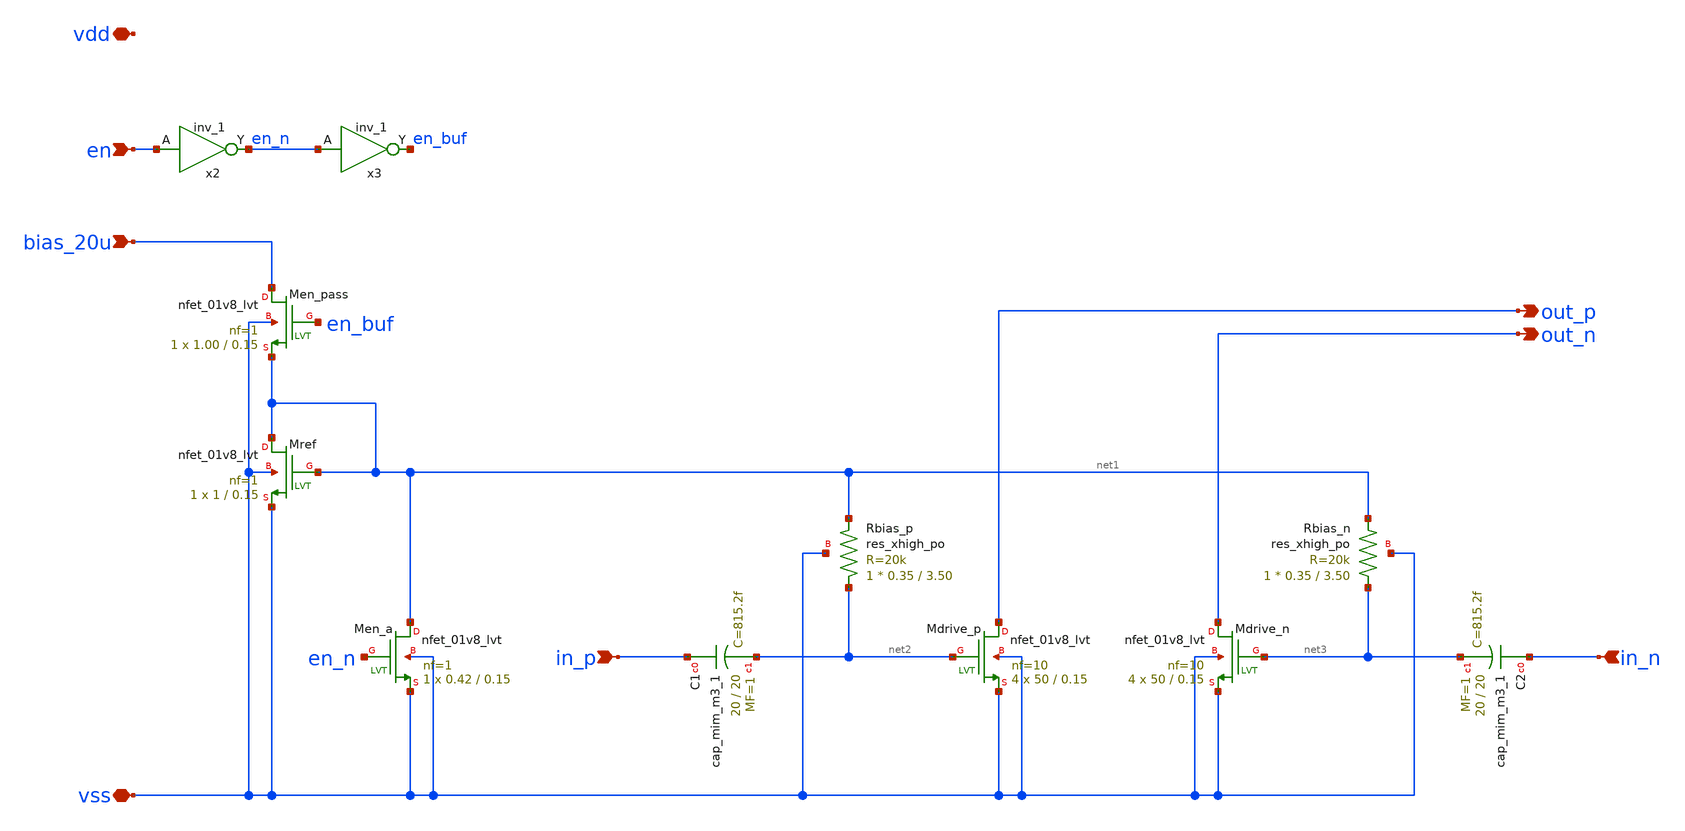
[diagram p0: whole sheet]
** sch_path: design/io_driver/io_driver.sch
**.subckt io_driver en bias_20u vss vdd out_p out_n in_n in_p
*.ipin en
*.ipin bias_20u
*.iopin vss
*.iopin vdd
*.opin out_p
*.opin out_n
*.ipin in_n
*.ipin in_p
XMdrive_p out_p net2 vss vss sky130_fd_pr__nfet_01v8_lvt L=0.15 W=50 nf=10 ad='int((nf+1)/2) * W/nf * 0.29'
+ as='int((nf+2)/2) * W/nf * 0.29' pd='2*int((nf+1)/2) * (W/nf + 0.29)' ps='2*int((nf+2)/2) * (W/nf + 0.29)'
+ nrd='0.29 / W' nrs='0.29 / W' sa=0 sb=0 sd=0 mult=4 m=4
XMdrive_n out_n net3 vss vss sky130_fd_pr__nfet_01v8_lvt L=0.15 W=50 nf=10 ad='int((nf+1)/2) * W/nf * 0.29'
+ as='int((nf+2)/2) * W/nf * 0.29' pd='2*int((nf+1)/2) * (W/nf + 0.29)' ps='2*int((nf+2)/2) * (W/nf + 0.29)'
+ nrd='0.29 / W' nrs='0.29 / W' sa=0 sb=0 sd=0 mult=4 m=4
XMref net1 net1 vss vss sky130_fd_pr__nfet_01v8_lvt L=0.15 W=1 nf=1 ad='int((nf+1)/2) * W/nf * 0.29'
+ as='int((nf+2)/2) * W/nf * 0.29' pd='2*int((nf+1)/2) * (W/nf + 0.29)' ps='2*int((nf+2)/2) * (W/nf + 0.29)'
+ nrd='0.29 / W' nrs='0.29 / W' sa=0 sb=0 sd=0 mult=1 m=1
XMen_pass bias_20u en_buf net1 vss sky130_fd_pr__nfet_01v8_lvt L=0.15 W=1.00 nf=1 ad='int((nf+1)/2) * W/nf * 0.29'
+ as='int((nf+2)/2) * W/nf * 0.29' pd='2*int((nf+1)/2) * (W/nf + 0.29)' ps='2*int((nf+2)/2) * (W/nf + 0.29)'
+ nrd='0.29 / W' nrs='0.29 / W' sa=0 sb=0 sd=0 mult=1 m=1
XMen_a net1 en_n vss vss sky130_fd_pr__nfet_01v8_lvt L=0.15 W=0.42 nf=1 ad='int((nf+1)/2) * W/nf * 0.29'
+ as='int((nf+2)/2) * W/nf * 0.29' pd='2*int((nf+1)/2) * (W/nf + 0.29)' ps='2*int((nf+2)/2) * (W/nf + 0.29)'
+ nrd='0.29 / W' nrs='0.29 / W' sa=0 sb=0 sd=0 mult=1 m=1
x2 en vss vss vdd vdd en_n sky130_fd_sc_hs__inv_1
x3 en_n vss vss vdd vdd en_buf sky130_fd_sc_hs__inv_1
XC1 in_p net2 sky130_fd_pr__cap_mim_m3_1 W=20 L=20 MF=1 m=1
XC2 in_n net3 sky130_fd_pr__cap_mim_m3_1 W=20 L=20 MF=1 m=1
XRbias_p net2 net1 vss sky130_fd_pr__res_xhigh_po W=0.35 L=3.50 mult=1 m=1
XRbias_n net3 net1 vss sky130_fd_pr__res_xhigh_po W=0.35 L=3.50 mult=1 m=1
**.ends
.end
